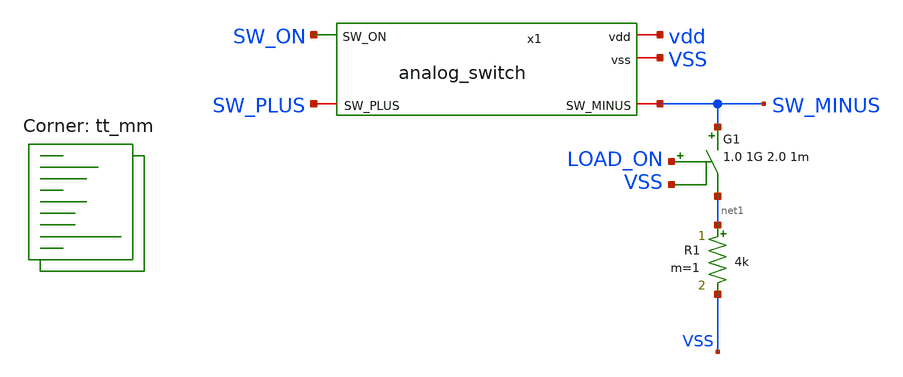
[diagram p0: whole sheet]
** sch_path: xschem/analog_switch_tb.sch
**.subckt analog_switch_tb
R1 net1 VSS 4k m=1
G1 SW_MINUS net1 vcr pwl(1) LOAD_ON VSS 1.0 1G 2.0 1m
x1 vdd VSS SW_ON SW_PLUS SW_MINUS analog_switch
**** begin user architecture code
.lib $::SKYWATER_MODELS/sky130.lib.spice tt_mm

*.option method = gear
*.option wnflag = 1
.param VCC = agauss(1.8,0.5,1)
.param w_swfet = 16
.option temp = aguass(40,30,1)
.include stimuli_tb_analog_switch.cir
.control
	option seed = 69
	let run = 0
	dowhile run <= 100
		save all
		tran 1n 8u uic
		remzerovec
		write tb_analog_switch_tran.raw
		set appendwrite
		reset
		let run = run +1
	end
.endc



**** end user architecture code
**.ends
.end
